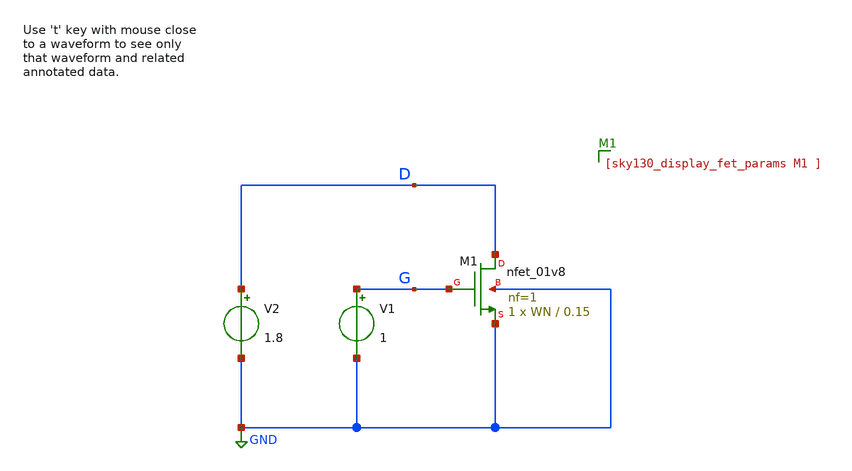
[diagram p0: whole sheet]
** sch_path: sky130A/xschem_libs/sky130_tests_ase/test_sweep_mos_w/schematic/test_sweep_mos_w.sch
* Copyright 2021 Stefan Frederik Schippers
* Licensed under the Apache License, Version 2.0 (the "License");
* you may not use this file except in compliance with the License.
* You may obtain a copy of the License at
* https://www.apache.org/licenses/LICENSE-2.0
* Unless required by applicable law or agreed to in writing, software
* distributed under the License is distributed on an "AS IS" BASIS,
* WITHOUT WARRANTIES OR CONDITIONS OF ANY KIND, either express or implied.
* See the License for the specific language governing permissions and
* limitations under the License.
**.subckt test_sweep_mos_w
V1 G GND 1
V2 D GND 1.8
XM1 D G GND GND sky130_fd_pr__nfet_01v8 L=0.15 W=WN nf=1 ad='int((1 + 1)/2) * WN / 1 * 0.29' as='int((1 + 2)/2) * WN / 1 * 0.29'
+ pd='2*int((1 + 1)/2) * (WN / 1 + 0.29)' ps='2*int((1 + 2)/2) * (WN / 1 + 0.29)' nrd='0.29 / WN ' nrs='0.29 / WN '
+ sa=0 sb=0 sd=0 mult=1 m=1
**.ends
.GLOBAL GND
.end
